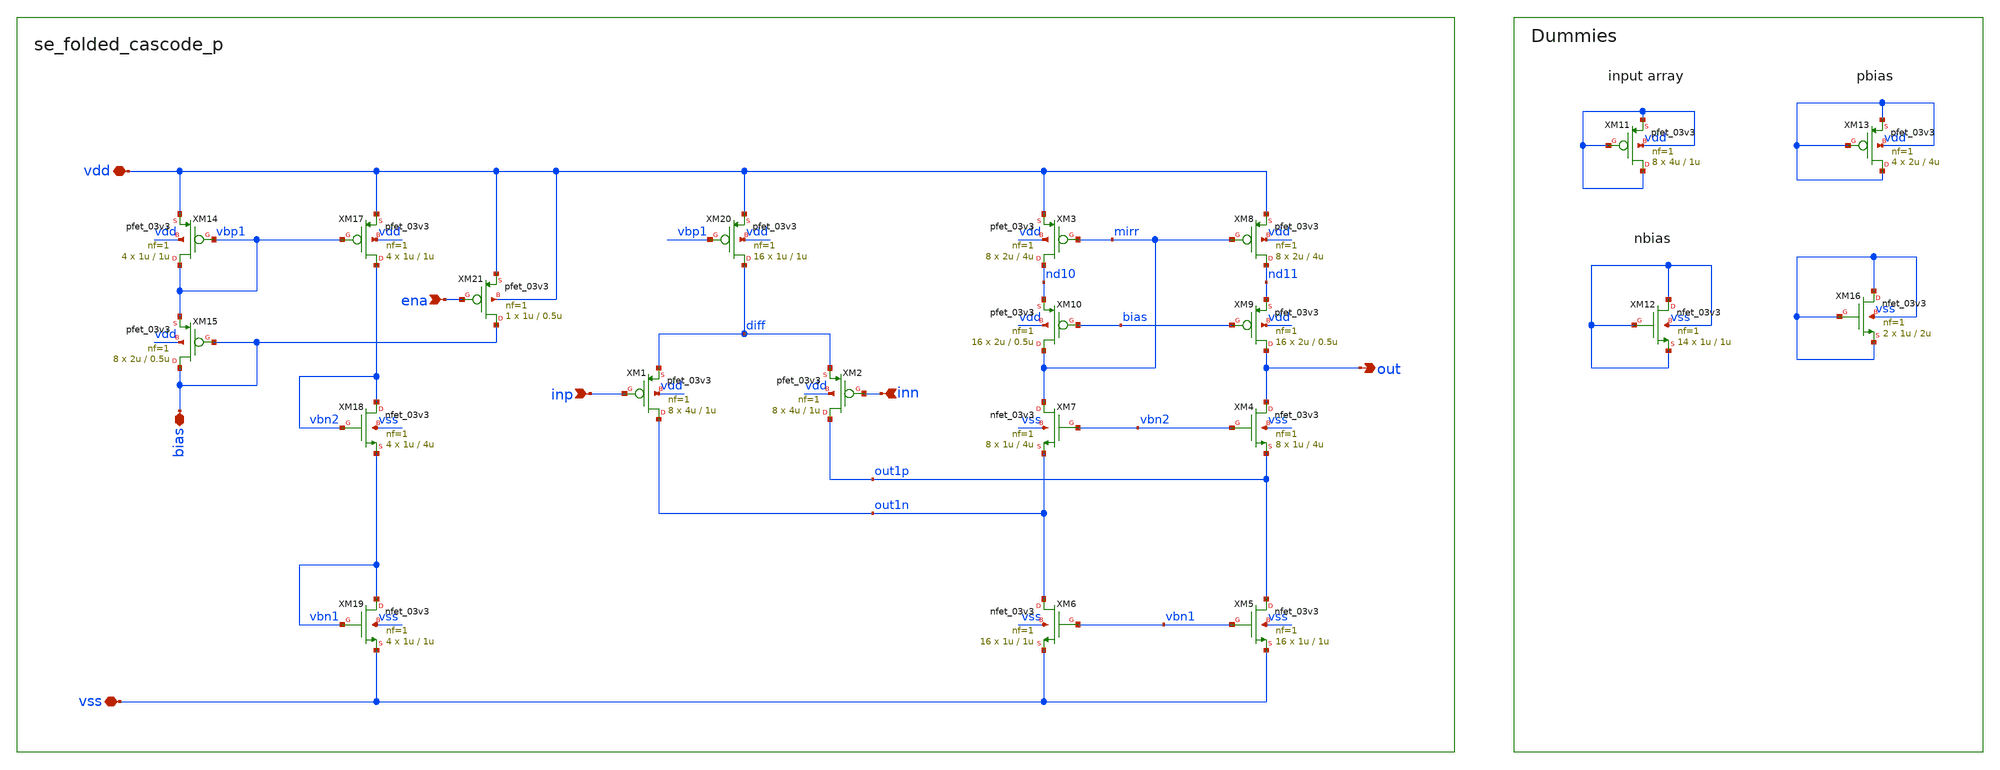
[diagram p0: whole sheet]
** sch_path: projects/programmable_transceiver_platform/analog/core_support/bandgap/xschem/se_folded_cascode_p.sch
**.subckt se_folded_cascode_p inn inp out bias vdd vss ena
*.ipin inn
*.ipin inp
*.opin out
*.iopin bias
*.iopin vdd
*.iopin vss
*.ipin ena
XM14 vbp1 vbp1 vdd vdd pfet_03v3 L=1u W=1u nf=1 ad='int((nf+1)/2) * W/nf * 0.18u' as='int((nf+2)/2) * W/nf * 0.18u'
+ pd='2*int((nf+1)/2) * (W/nf + 0.18u)' ps='2*int((nf+2)/2) * (W/nf + 0.18u)' nrd='0.18u / W' nrs='0.18u / W'
+ sa=0 sb=0 sd=0 m=4 par=4
XM15 bias bias vbp1 vdd pfet_03v3 L=0.5u W=2u nf=1 ad='int((nf+1)/2) * W/nf * 0.18u' as='int((nf+2)/2) * W/nf * 0.18u'
+ pd='2*int((nf+1)/2) * (W/nf + 0.18u)' ps='2*int((nf+2)/2) * (W/nf + 0.18u)' nrd='0.18u / W' nrs='0.18u / W'
+ sa=0 sb=0 sd=0 m=8 par=8
XM17 vbn2 vbp1 vdd vdd pfet_03v3 L=1u W=1u nf=1 ad='int((nf+1)/2) * W/nf * 0.18u' as='int((nf+2)/2) * W/nf * 0.18u'
+ pd='2*int((nf+1)/2) * (W/nf + 0.18u)' ps='2*int((nf+2)/2) * (W/nf + 0.18u)' nrd='0.18u / W' nrs='0.18u / W'
+ sa=0 sb=0 sd=0 m=4 par=4
XM18 vbn2 vbn2 vbn1 vss nfet_03v3 L=4u W=1u nf=1 ad='int((nf+1)/2) * W/nf * 0.18u' as='int((nf+2)/2) * W/nf * 0.18u'
+ pd='2*int((nf+1)/2) * (W/nf + 0.18u)' ps='2*int((nf+2)/2) * (W/nf + 0.18u)' nrd='0.18u / W' nrs='0.18u / W'
+ sa=0 sb=0 sd=0 m=4 par=4
XM19 vbn1 vbn1 vss vss nfet_03v3 L=1u W=1u nf=1 ad='int((nf+1)/2) * W/nf * 0.18u' as='int((nf+2)/2) * W/nf * 0.18u'
+ pd='2*int((nf+1)/2) * (W/nf + 0.18u)' ps='2*int((nf+2)/2) * (W/nf + 0.18u)' nrd='0.18u / W' nrs='0.18u / W'
+ sa=0 sb=0 sd=0 m=4 par=4
XM20 diff vbp1 vdd vdd pfet_03v3 L=1u W=1u nf=1 ad='int((nf+1)/2) * W/nf * 0.18u' as='int((nf+2)/2) * W/nf * 0.18u'
+ pd='2*int((nf+1)/2) * (W/nf + 0.18u)' ps='2*int((nf+2)/2) * (W/nf + 0.18u)' nrd='0.18u / W' nrs='0.18u / W'
+ sa=0 sb=0 sd=0 m=16 par=16
XM1 out1n inp diff vdd pfet_03v3 L=1u W=4u nf=1 ad='int((nf+1)/2) * W/nf * 0.18u' as='int((nf+2)/2) * W/nf * 0.18u'
+ pd='2*int((nf+1)/2) * (W/nf + 0.18u)' ps='2*int((nf+2)/2) * (W/nf + 0.18u)' nrd='0.18u / W' nrs='0.18u / W'
+ sa=0 sb=0 sd=0 m=8 par=8
XM2 out1p inn diff vdd pfet_03v3 L=1u W=4u nf=1 ad='int((nf+1)/2) * W/nf * 0.18u' as='int((nf+2)/2) * W/nf * 0.18u'
+ pd='2*int((nf+1)/2) * (W/nf + 0.18u)' ps='2*int((nf+2)/2) * (W/nf + 0.18u)' nrd='0.18u / W' nrs='0.18u / W'
+ sa=0 sb=0 sd=0 m=8 par=8
XM3 nd10 mirr vdd vdd pfet_03v3 L=4u W=2u nf=1 ad='int((nf+1)/2) * W/nf * 0.18u' as='int((nf+2)/2) * W/nf * 0.18u'
+ pd='2*int((nf+1)/2) * (W/nf + 0.18u)' ps='2*int((nf+2)/2) * (W/nf + 0.18u)' nrd='0.18u / W' nrs='0.18u / W'
+ sa=0 sb=0 sd=0 m=8 par=8
XM8 nd11 mirr vdd vdd pfet_03v3 L=4u W=2u nf=1 ad='int((nf+1)/2) * W/nf * 0.18u' as='int((nf+2)/2) * W/nf * 0.18u'
+ pd='2*int((nf+1)/2) * (W/nf + 0.18u)' ps='2*int((nf+2)/2) * (W/nf + 0.18u)' nrd='0.18u / W' nrs='0.18u / W'
+ sa=0 sb=0 sd=0 m=8 par=8
XM9 out bias nd11 vdd pfet_03v3 L=0.5u W=2u nf=1 ad='int((nf+1)/2) * W/nf * 0.18u' as='int((nf+2)/2) * W/nf * 0.18u'
+ pd='2*int((nf+1)/2) * (W/nf + 0.18u)' ps='2*int((nf+2)/2) * (W/nf + 0.18u)' nrd='0.18u / W' nrs='0.18u / W'
+ sa=0 sb=0 sd=0 m=16 par=16
XM10 mirr bias nd10 vdd pfet_03v3 L=0.5u W=2u nf=1 ad='int((nf+1)/2) * W/nf * 0.18u' as='int((nf+2)/2) * W/nf * 0.18u'
+ pd='2*int((nf+1)/2) * (W/nf + 0.18u)' ps='2*int((nf+2)/2) * (W/nf + 0.18u)' nrd='0.18u / W' nrs='0.18u / W'
+ sa=0 sb=0 sd=0 m=16 par=16
XM4 out vbn2 out1p vss nfet_03v3 L=4u W=1u nf=1 ad='int((nf+1)/2) * W/nf * 0.18u' as='int((nf+2)/2) * W/nf * 0.18u'
+ pd='2*int((nf+1)/2) * (W/nf + 0.18u)' ps='2*int((nf+2)/2) * (W/nf + 0.18u)' nrd='0.18u / W' nrs='0.18u / W'
+ sa=0 sb=0 sd=0 m=8 par=8
XM5 out1p vbn1 vss vss nfet_03v3 L=1u W=1u nf=1 ad='int((nf+1)/2) * W/nf * 0.18u' as='int((nf+2)/2) * W/nf * 0.18u'
+ pd='2*int((nf+1)/2) * (W/nf + 0.18u)' ps='2*int((nf+2)/2) * (W/nf + 0.18u)' nrd='0.18u / W' nrs='0.18u / W'
+ sa=0 sb=0 sd=0 m=16 par=16
XM6 out1n vbn1 vss vss nfet_03v3 L=1u W=1u nf=1 ad='int((nf+1)/2) * W/nf * 0.18u' as='int((nf+2)/2) * W/nf * 0.18u'
+ pd='2*int((nf+1)/2) * (W/nf + 0.18u)' ps='2*int((nf+2)/2) * (W/nf + 0.18u)' nrd='0.18u / W' nrs='0.18u / W'
+ sa=0 sb=0 sd=0 m=16 par=16
XM7 mirr vbn2 out1n vss nfet_03v3 L=4u W=1u nf=1 ad='int((nf+1)/2) * W/nf * 0.18u' as='int((nf+2)/2) * W/nf * 0.18u'
+ pd='2*int((nf+1)/2) * (W/nf + 0.18u)' ps='2*int((nf+2)/2) * (W/nf + 0.18u)' nrd='0.18u / W' nrs='0.18u / W'
+ sa=0 sb=0 sd=0 m=8 par=8
XM11 vdd vdd vdd vdd pfet_03v3 L=1u W=4u nf=1 ad='int((nf+1)/2) * W/nf * 0.18u' as='int((nf+2)/2) * W/nf * 0.18u'
+ pd='2*int((nf+1)/2) * (W/nf + 0.18u)' ps='2*int((nf+2)/2) * (W/nf + 0.18u)' nrd='0.18u / W' nrs='0.18u / W'
+ sa=0 sb=0 sd=0 m=8 par=8
XM12 vss vss vss vss nfet_03v3 L=1u W=1u nf=1 ad='int((nf+1)/2) * W/nf * 0.18u' as='int((nf+2)/2) * W/nf * 0.18u'
+ pd='2*int((nf+1)/2) * (W/nf + 0.18u)' ps='2*int((nf+2)/2) * (W/nf + 0.18u)' nrd='0.18u / W' nrs='0.18u / W'
+ sa=0 sb=0 sd=0 m=14 par=14
XM13 vdd vdd vdd vdd pfet_03v3 L=4u W=2u nf=1 ad='int((nf+1)/2) * W/nf * 0.18u' as='int((nf+2)/2) * W/nf * 0.18u'
+ pd='2*int((nf+1)/2) * (W/nf + 0.18u)' ps='2*int((nf+2)/2) * (W/nf + 0.18u)' nrd='0.18u / W' nrs='0.18u / W'
+ sa=0 sb=0 sd=0 m=4 par=4
XM21 bias ena vdd vdd pfet_03v3 L=0.5u W=1u nf=1 ad='int((nf+1)/2) * W/nf * 0.18u' as='int((nf+2)/2) * W/nf * 0.18u'
+ pd='2*int((nf+1)/2) * (W/nf + 0.18u)' ps='2*int((nf+2)/2) * (W/nf + 0.18u)' nrd='0.18u / W' nrs='0.18u / W'
+ sa=0 sb=0 sd=0 m=1 par=1
XM16 vss vss vss vss nfet_03v3 L=2u W=1u nf=1 ad='int((nf+1)/2) * W/nf * 0.18u' as='int((nf+2)/2) * W/nf * 0.18u'
+ pd='2*int((nf+1)/2) * (W/nf + 0.18u)' ps='2*int((nf+2)/2) * (W/nf + 0.18u)' nrd='0.18u / W' nrs='0.18u / W'
+ sa=0 sb=0 sd=0 m=2 par=2
**.ends
.end
